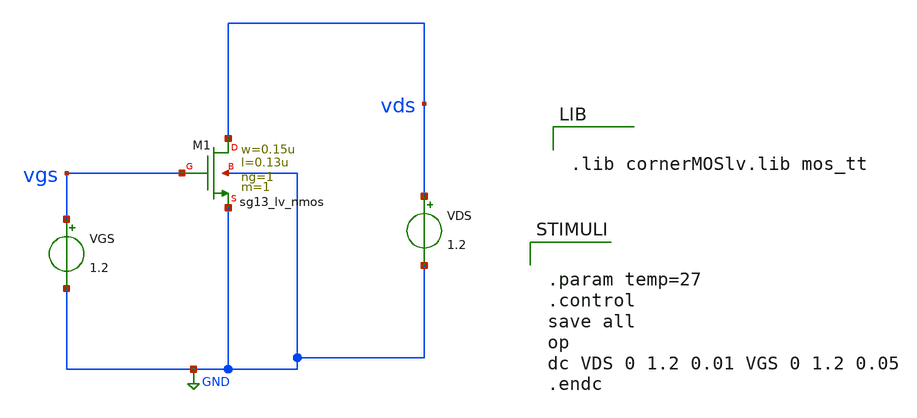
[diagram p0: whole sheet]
** sch_path: lab2-1.sch
**.subckt lab2-1
VGS vgs GND 1.2
XM1 vds vgs GND GND sg13_lv_nmos w=0.15u l=0.13u ng=1 m=1 mm_ok=1
VDS vds GND 1.2
**** begin user architecture code


.lib cornerMOSlv.lib mos_tt



.param temp=27
.control
save all
op
dc VDS 0 1.2 0.01 VGS 0 1.2 0.05
.endc


**** end user architecture code
**.ends
.GLOBAL GND
.end
